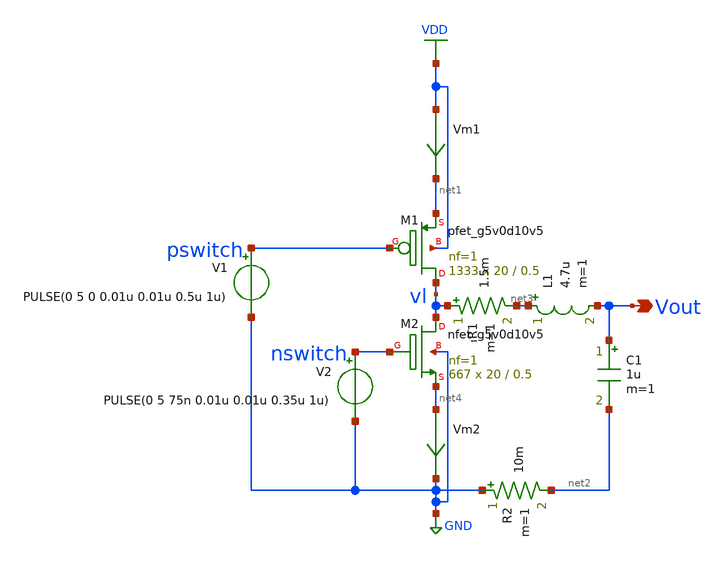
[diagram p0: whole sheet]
** sch_path: Ene_Thompson/Buck.sch
**.subckt Buck Vout
*.opin Vout
XM1 vl pswitch net1 VDD sky130_fd_pr__pfet_g5v0d10v5 L=0.5 W=20 nf=1 ad='int((nf+1)/2) * W/nf * 0.29'
+ as='int((nf+2)/2) * W/nf * 0.29' pd='2*int((nf+1)/2) * (W/nf + 0.29)' ps='2*int((nf+2)/2) * (W/nf + 0.29)'
+ nrd='0.29 / W' nrs='0.29 / W' sa=0 sb=0 sd=0 mult=1333 m=1333
XM2 vl nswitch net4 GND sky130_fd_pr__nfet_g5v0d10v5 L=0.5 W=20 nf=1 ad='int((nf+1)/2) * W/nf * 0.29'
+ as='int((nf+2)/2) * W/nf * 0.29' pd='2*int((nf+1)/2) * (W/nf + 0.29)' ps='2*int((nf+2)/2) * (W/nf + 0.29)'
+ nrd='0.29 / W' nrs='0.29 / W' sa=0 sb=0 sd=0 mult=667 m=667
L1 net3 Vout 4.7u m=1
C1 Vout net2 1u m=1
V1 pswitch GND PULSE(0 5 0 0.01u 0.01u 0.5u 1u)
R1 vl net3 1.5m m=1
R2 GND net2 10m m=1
V2 nswitch GND PULSE(0 5 75n 0.01u 0.01u 0.35u 1u)
Vm1 VDD net1 0
.save i(vm1)
Vm2 net4 GND 0
.save i(vm2)
**.ends
.GLOBAL GND
.GLOBAL VDD
.end
